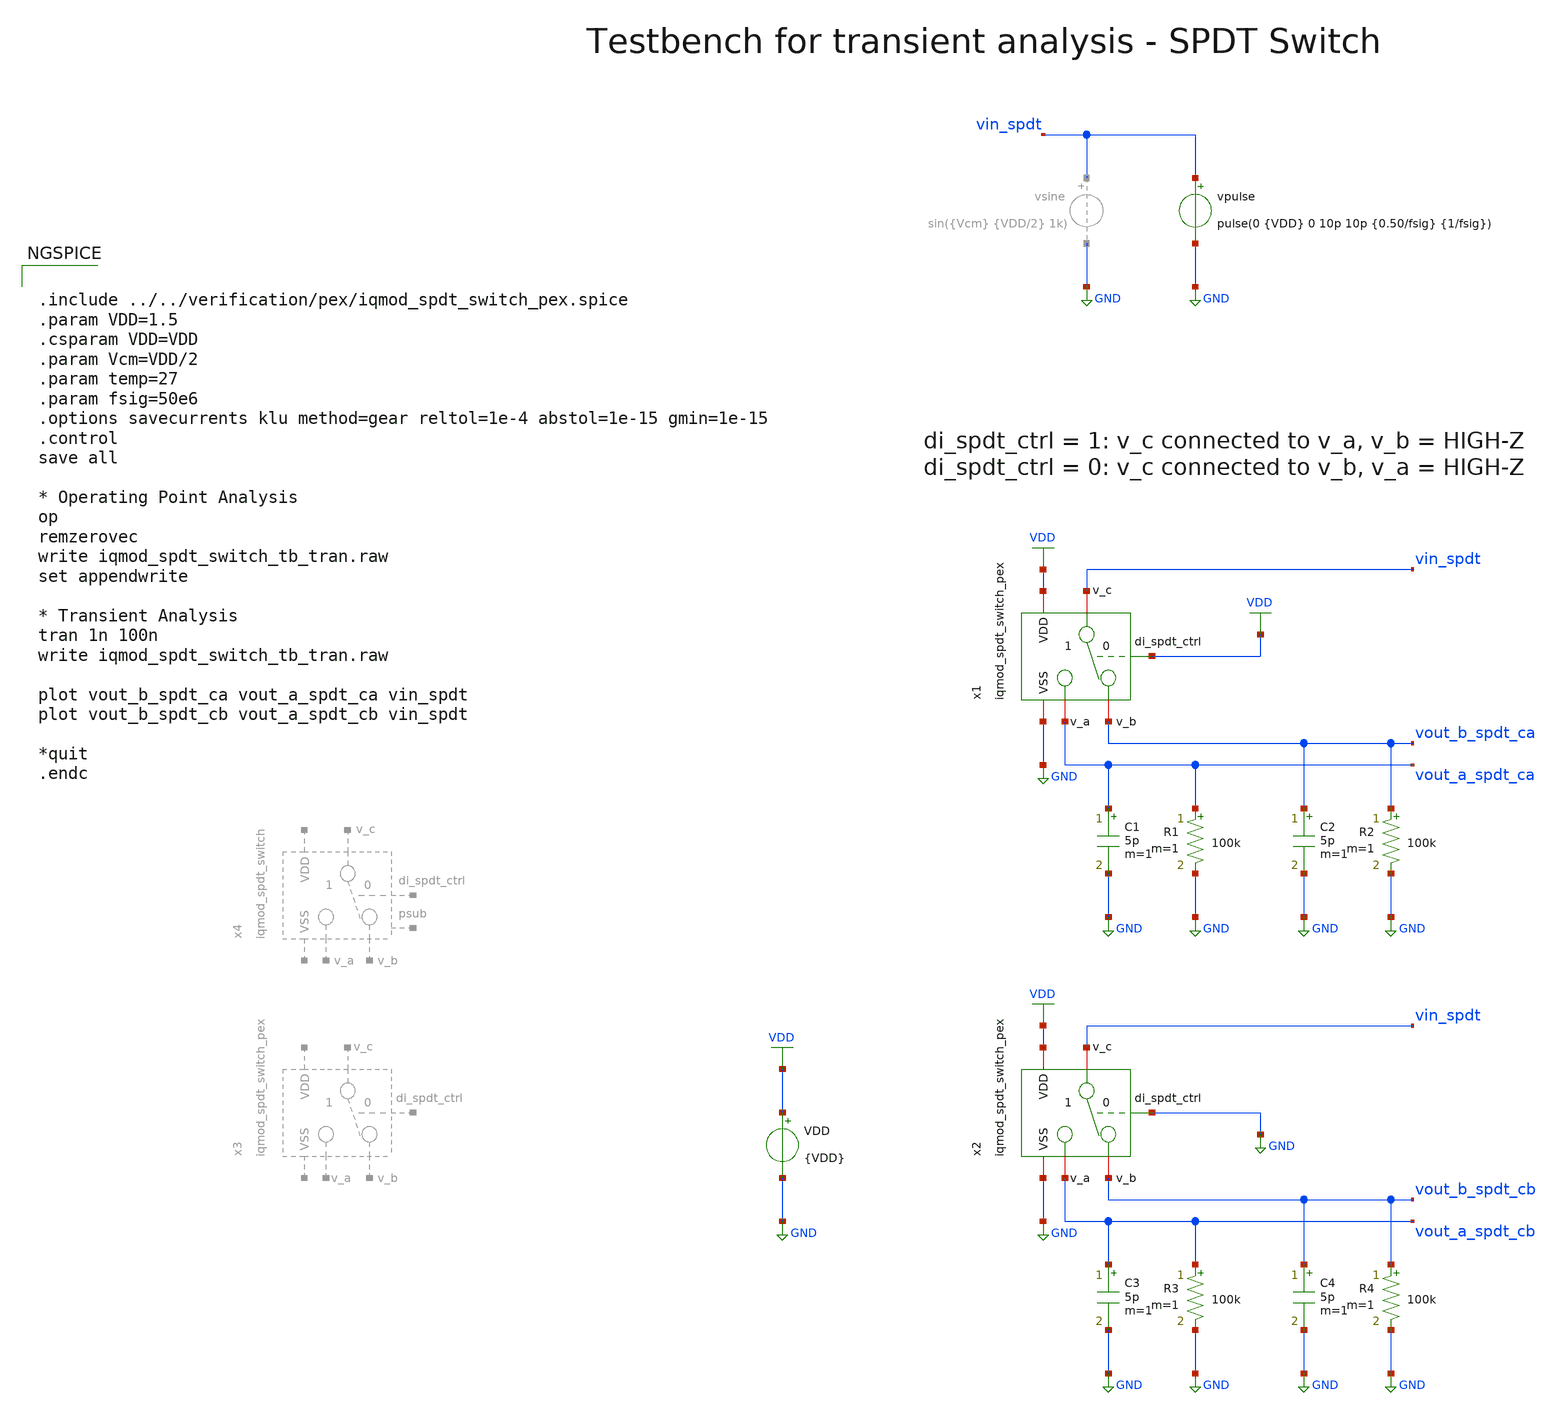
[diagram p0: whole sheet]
** sch_path: ihp130/macros/iqmod/xschem/testbenches/iqmod_spdt_switch_tb_tran.sch
**.subckt iqmod_spdt_switch_tb_tran
C1 vout_a_spdt_ca GND 5p m=1
VDD VDD GND {VDD}
C2 vout_b_spdt_ca GND 5p m=1
x1 VDD VDD GND vin_spdt vout_b_spdt_ca vout_a_spdt_ca iqmod_spdt_switch_pex
x2 VDD GND GND vin_spdt vout_b_spdt_cb vout_a_spdt_cb iqmod_spdt_switch_pex
vpulse vin_spdt GND pulse(0 {VDD} 0 10p 10p {0.50/fsig} {1/fsig})
R1 vout_a_spdt_ca GND 100k m=1
R2 vout_b_spdt_ca GND 100k m=1
C3 vout_a_spdt_cb GND 5p m=1
C4 vout_b_spdt_cb GND 5p m=1
R3 vout_a_spdt_cb GND 100k m=1
R4 vout_b_spdt_cb GND 100k m=1
**** begin user architecture code


.include ../../verification/pex/iqmod_spdt_switch_pex.spice
.param VDD=1.5
.csparam VDD=VDD
.param Vcm=VDD/2
.param temp=27
.param fsig=50e6
.options savecurrents klu method=gear reltol=1e-4 abstol=1e-15 gmin=1e-15
.control
save all

* Operating Point Analysis
op
remzerovec
write iqmod_spdt_switch_tb_tran.raw
set appendwrite

* Transient Analysis
tran 1n 100n
write iqmod_spdt_switch_tb_tran.raw

plot vout_b_spdt_ca vout_a_spdt_ca vin_spdt
plot vout_b_spdt_cb vout_a_spdt_cb vin_spdt

*quit
.endc


.lib cornerMOSlv.lib mos_tt
.lib cornerMOShv.lib mos_tt
.lib cornerHBT.lib hbt_typ
.lib cornerRES.lib res_typ
.lib cornerCAP.lib cap_typ
.lib cornerDIO.lib dio_tt

**** end user architecture code
**.ends
.GLOBAL VDD
.GLOBAL GND
.end
